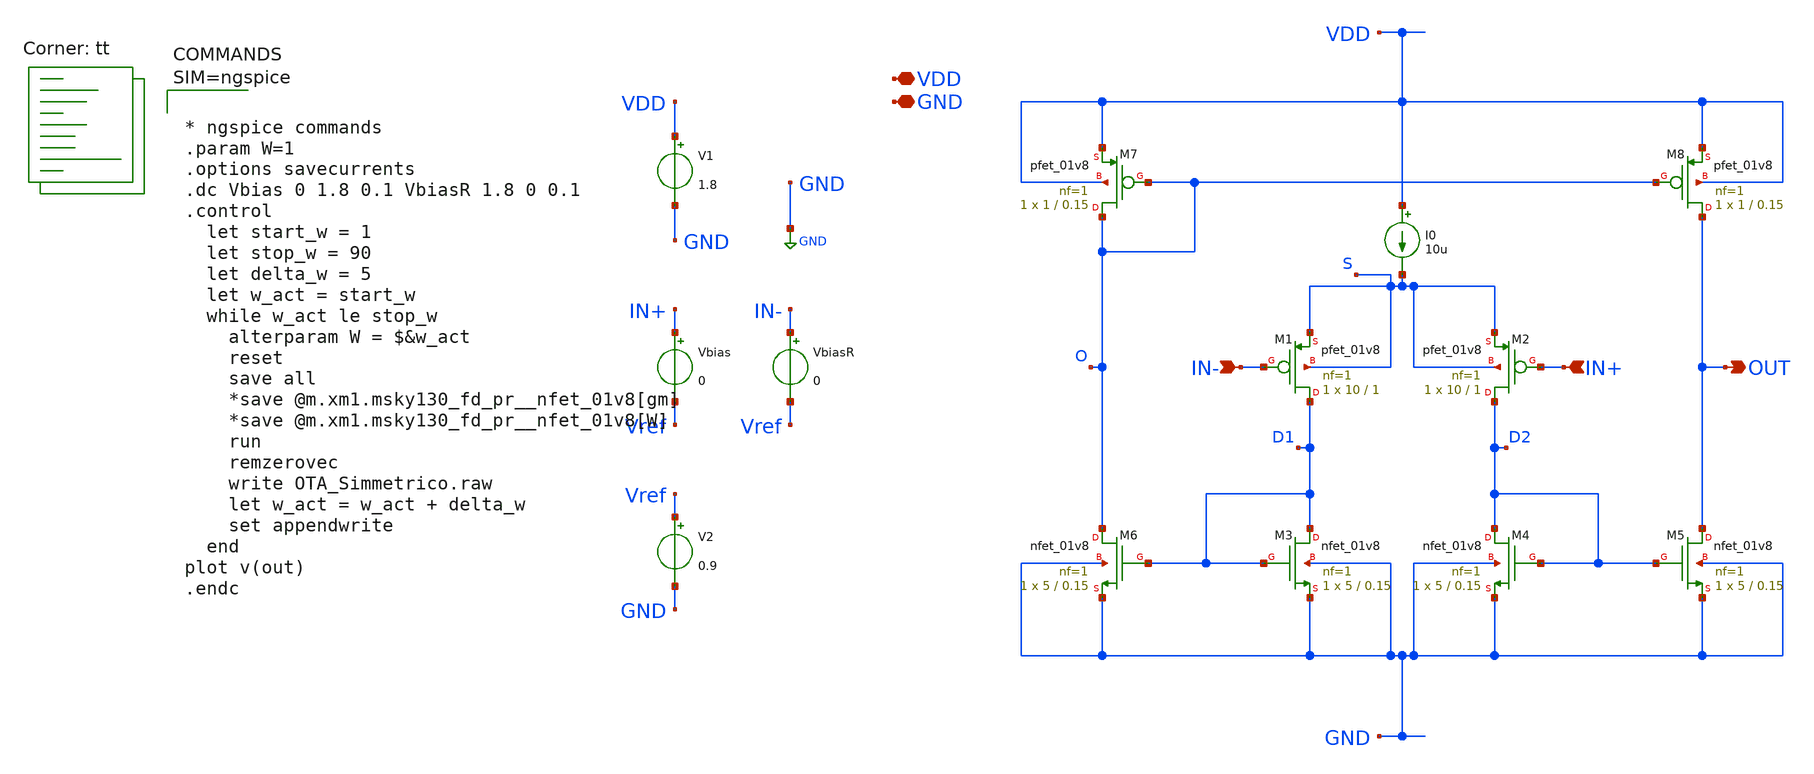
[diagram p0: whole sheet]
** sch_path: xschem/OTA_Simmetrico.sch
**.subckt OTA_Simmetrico VDD GND IN+ IN- OUT
*.iopin VDD
*.iopin GND
*.ipin IN+
*.ipin IN-
*.opin OUT
XM1 D1 IN- S S sky130_fd_pr__pfet_01v8 L=1 W=10 nf=1 ad='int((nf+1)/2) * W/nf * 0.29' as='int((nf+2)/2) * W/nf * 0.29'
+ pd='2*int((nf+1)/2) * (W/nf + 0.29)' ps='2*int((nf+2)/2) * (W/nf + 0.29)' nrd='0.29 / W' nrs='0.29 / W'
+ sa=0 sb=0 sd=0 mult=1 m=1
XM2 D2 IN+ S S sky130_fd_pr__pfet_01v8 L=1 W=10 nf=1 ad='int((nf+1)/2) * W/nf * 0.29' as='int((nf+2)/2) * W/nf * 0.29'
+ pd='2*int((nf+1)/2) * (W/nf + 0.29)' ps='2*int((nf+2)/2) * (W/nf + 0.29)' nrd='0.29 / W' nrs='0.29 / W'
+ sa=0 sb=0 sd=0 mult=1 m=1
XM3 D1 D1 GND GND sky130_fd_pr__nfet_01v8 L=0.15 W=5 nf=1 ad='int((nf+1)/2) * W/nf * 0.29' as='int((nf+2)/2) * W/nf * 0.29'
+ pd='2*int((nf+1)/2) * (W/nf + 0.29)' ps='2*int((nf+2)/2) * (W/nf + 0.29)' nrd='0.29 / W' nrs='0.29 / W'
+ sa=0 sb=0 sd=0 mult=1 m=1
XM4 D2 D2 GND GND sky130_fd_pr__nfet_01v8 L=0.15 W=5 nf=1 ad='int((nf+1)/2) * W/nf * 0.29' as='int((nf+2)/2) * W/nf * 0.29'
+ pd='2*int((nf+1)/2) * (W/nf + 0.29)' ps='2*int((nf+2)/2) * (W/nf + 0.29)' nrd='0.29 / W' nrs='0.29 / W'
+ sa=0 sb=0 sd=0 mult=1 m=1
XM5 OUT D2 GND GND sky130_fd_pr__nfet_01v8 L=0.15 W=5 nf=1 ad='int((nf+1)/2) * W/nf * 0.29' as='int((nf+2)/2) * W/nf * 0.29'
+ pd='2*int((nf+1)/2) * (W/nf + 0.29)' ps='2*int((nf+2)/2) * (W/nf + 0.29)' nrd='0.29 / W' nrs='0.29 / W'
+ sa=0 sb=0 sd=0 mult=1 m=1
XM6 O D1 GND GND sky130_fd_pr__nfet_01v8 L=0.15 W=5 nf=1 ad='int((nf+1)/2) * W/nf * 0.29' as='int((nf+2)/2) * W/nf * 0.29'
+ pd='2*int((nf+1)/2) * (W/nf + 0.29)' ps='2*int((nf+2)/2) * (W/nf + 0.29)' nrd='0.29 / W' nrs='0.29 / W'
+ sa=0 sb=0 sd=0 mult=1 m=1
XM7 O O VDD VDD sky130_fd_pr__pfet_01v8 L=0.15 W=1 nf=1 ad='int((nf+1)/2) * W/nf * 0.29' as='int((nf+2)/2) * W/nf * 0.29'
+ pd='2*int((nf+1)/2) * (W/nf + 0.29)' ps='2*int((nf+2)/2) * (W/nf + 0.29)' nrd='0.29 / W' nrs='0.29 / W'
+ sa=0 sb=0 sd=0 mult=1 m=1
XM8 OUT O VDD VDD sky130_fd_pr__pfet_01v8 L=0.15 W=1 nf=1 ad='int((nf+1)/2) * W/nf * 0.29' as='int((nf+2)/2) * W/nf * 0.29'
+ pd='2*int((nf+1)/2) * (W/nf + 0.29)' ps='2*int((nf+2)/2) * (W/nf + 0.29)' nrd='0.29 / W' nrs='0.29 / W'
+ sa=0 sb=0 sd=0 mult=1 m=1
I0 VDD S 10u
V1 VDD GND 1.8
Vbias IN+ Vref 0
VbiasR IN- Vref 0
V2 Vref GND 0.9
**** begin user architecture code



* ngspice commands
.param W=1
.options savecurrents
.dc Vbias 0 1.8 0.1 VbiasR 1.8 0 0.1
.control
  let start_w = 1
  let stop_w = 90
  let delta_w = 5
  let w_act = start_w
  while w_act le stop_w
    alterparam W = $&w_act
    reset
    save all
    *save @m.xm1.msky130_fd_pr__nfet_01v8[gm]
    *save @m.xm1.msky130_fd_pr__nfet_01v8[W]
    run
    remzerovec
    write OTA_Simmetrico.raw
    let w_act = w_act + delta_w
    set appendwrite
  end
plot v(out)
.endc



.lib $::SKYWATER_MODELS/sky130.lib.spice tt
**** end user architecture code
**.ends
.GLOBAL GND
.end
